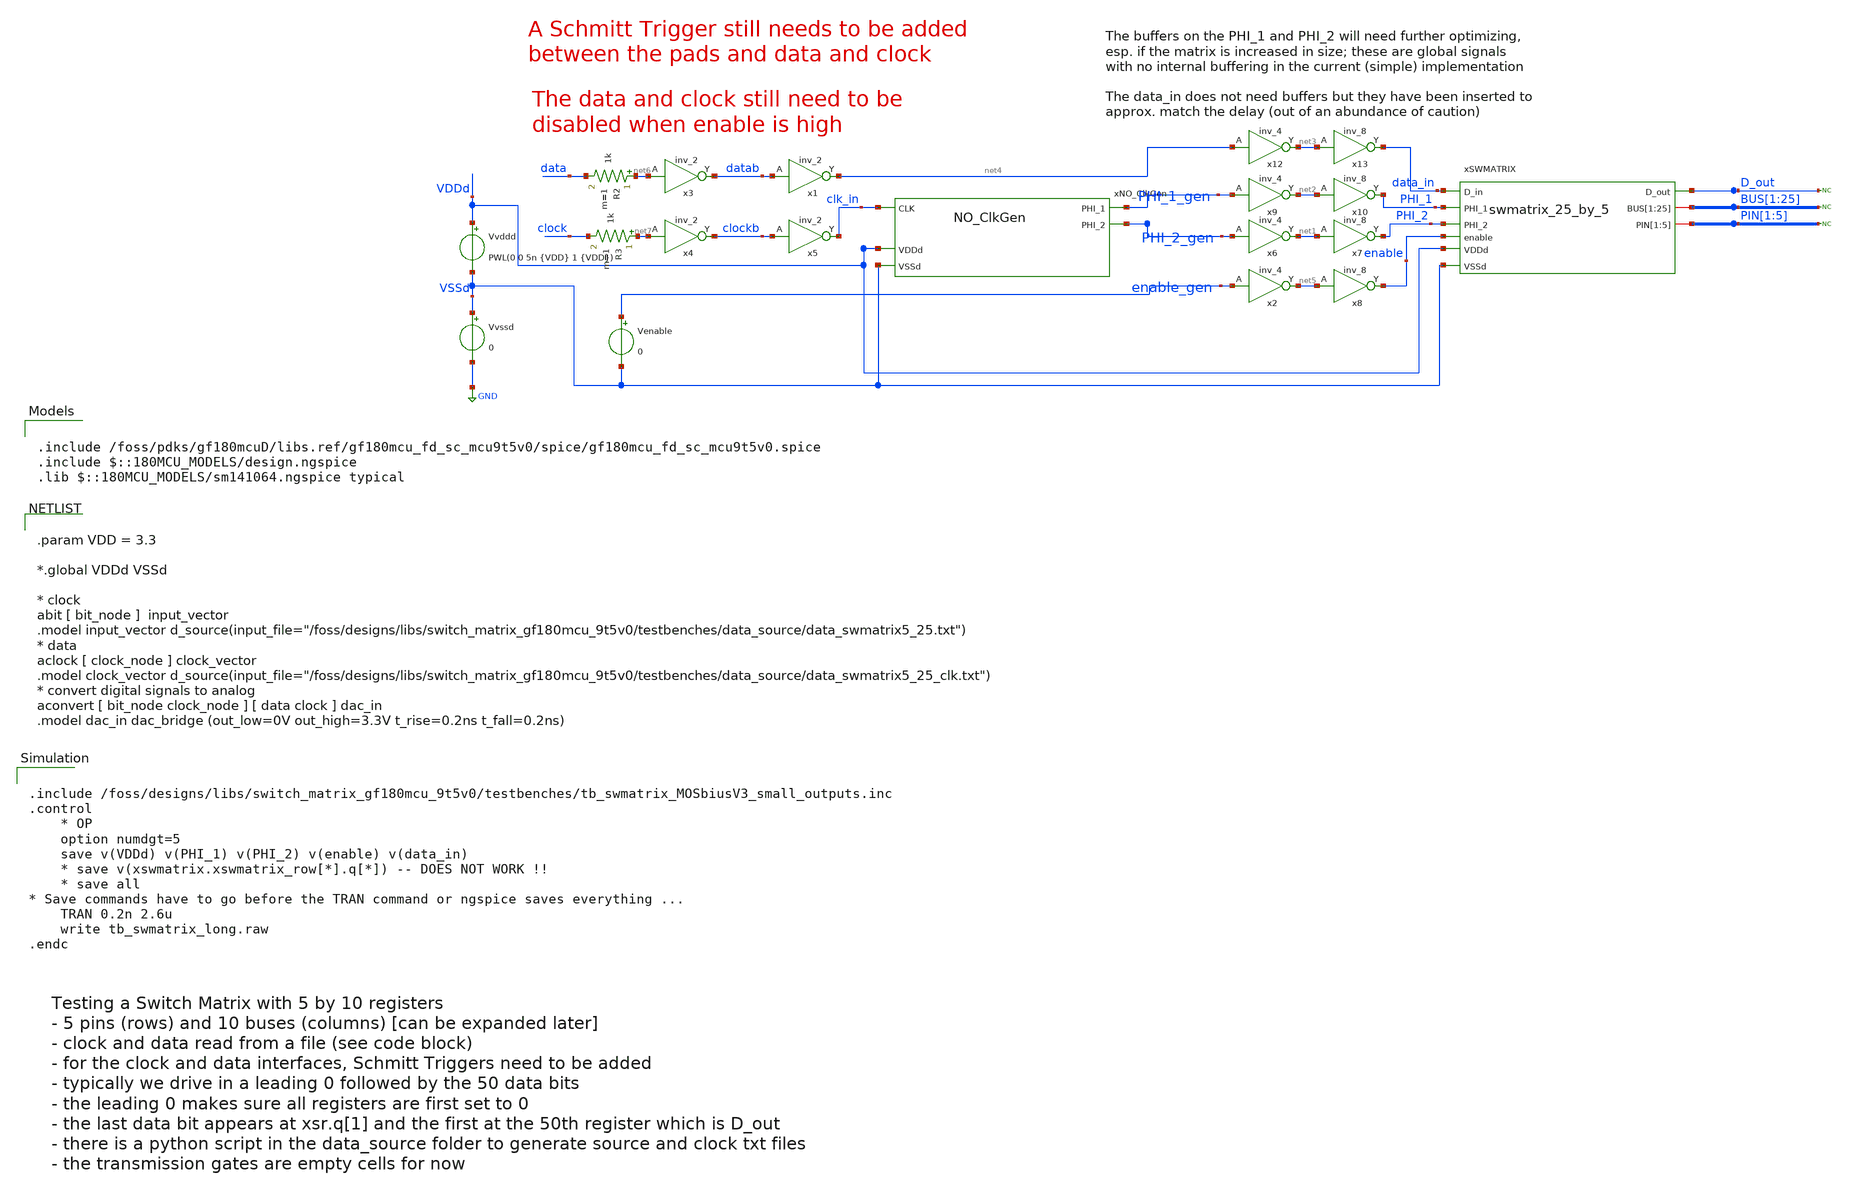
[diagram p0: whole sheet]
** sch_path: testbenches/tb_swmatrix_MOSbiusV3_small.sch
**.subckt tb_swmatrix_MOSbiusV3_small
Vvssd VSSd GND 0
Vvddd VDDd VSSd PWL(0 0 5n {VDD} 1 {VDD})
xNO_ClkGen PHI_2_gen clk_in PHI_1_gen VDDd VSSd NO_ClkGen
x3 net6 VSSd VDDd VSSd VDDd datab gf180mcu_fd_sc_mcu9t5v0__inv_2
x1 datab VSSd VDDd VSSd VDDd net4 gf180mcu_fd_sc_mcu9t5v0__inv_2
x4 net7 VSSd VDDd VSSd VDDd clockb gf180mcu_fd_sc_mcu9t5v0__inv_2
x5 clockb VSSd VDDd VSSd VDDd clk_in gf180mcu_fd_sc_mcu9t5v0__inv_2
* noconn D_out
* noconn BUS[1:25]
* noconn PIN[1:5]
x6 PHI_2_gen VSSd VDDd VSSd VDDd net1 gf180mcu_fd_sc_mcu9t5v0__inv_4
x7 net1 VSSd VDDd VSSd VDDd PHI_2 gf180mcu_fd_sc_mcu9t5v0__inv_8
x9 PHI_1_gen VSSd VDDd VSSd VDDd net2 gf180mcu_fd_sc_mcu9t5v0__inv_4
x10 net2 VSSd VDDd VSSd VDDd PHI_1 gf180mcu_fd_sc_mcu9t5v0__inv_8
x12 net4 VSSd VDDd VSSd VDDd net3 gf180mcu_fd_sc_mcu9t5v0__inv_4
x13 net3 VSSd VDDd VSSd VDDd data_in gf180mcu_fd_sc_mcu9t5v0__inv_8
x2 enable_gen VSSd VDDd VSSd VDDd net5 gf180mcu_fd_sc_mcu9t5v0__inv_4
x8 net5 VSSd VDDd VSSd VDDd enable gf180mcu_fd_sc_mcu9t5v0__inv_8
Venable enable_gen VSSd 0
xSWMATRIX data_in D_out PHI_1 PHI_2 BUS[1] BUS[2] BUS[3] BUS[4] BUS[5] BUS[6] BUS[7] BUS[8] BUS[9]
+ BUS[10] BUS[11] BUS[12] BUS[13] BUS[14] BUS[15] BUS[16] BUS[17] BUS[18] BUS[19] BUS[20] BUS[21] BUS[22]
+ BUS[23] BUS[24] BUS[25] PIN[1] PIN[2] PIN[3] PIN[4] PIN[5] VDDd VSSd enable swmatrix_25_by_5
R2 net6 data 1k m=1
R3 net7 clock 1k m=1
**** begin user architecture code


.include /foss/designs/libs/switch_matrix_gf180mcu_9t5v0/testbenches/tb_swmatrix_MOSbiusV3_small_outputs.inc
.control
    * OP
    option numdgt=5
    save v(VDDd) v(PHI_1) v(PHI_2) v(enable) v(data_in)
    * save v(xswmatrix.xswmatrix_row[*].q[*]) -- DOES NOT WORK !!
    * save all
* Save commands have to go before the TRAN command or ngspice saves everything ...
    TRAN 0.2n 2.6u
    write tb_swmatrix_long.raw
.endc



.include /foss/pdks/gf180mcuD/libs.ref/gf180mcu_fd_sc_mcu9t5v0/spice/gf180mcu_fd_sc_mcu9t5v0.spice
.include $::180MCU_MODELS/design.ngspice
.lib $::180MCU_MODELS/sm141064.ngspice typical



.param VDD = 3.3

*.global VDDd VSSd

* clock
abit [ bit_node ]  input_vector
.model input_vector
+ d_source(input_file="/foss/designs/libs/switch_matrix_gf180mcu_9t5v0/testbenches/data_source/data_swmatrix5_25.txt")
* data
aclock [ clock_node ] clock_vector
.model clock_vector
+ d_source(input_file="/foss/designs/libs/switch_matrix_gf180mcu_9t5v0/testbenches/data_source/data_swmatrix5_25_clk.txt")
* convert digital signals to analog
aconvert [ bit_node clock_node ] [ data clock ] dac_in
.model dac_in dac_bridge (out_low=0V out_high=3.3V t_rise=0.2ns t_fall=0.2ns)


**** end user architecture code
**.ends
.GLOBAL GND
.end
